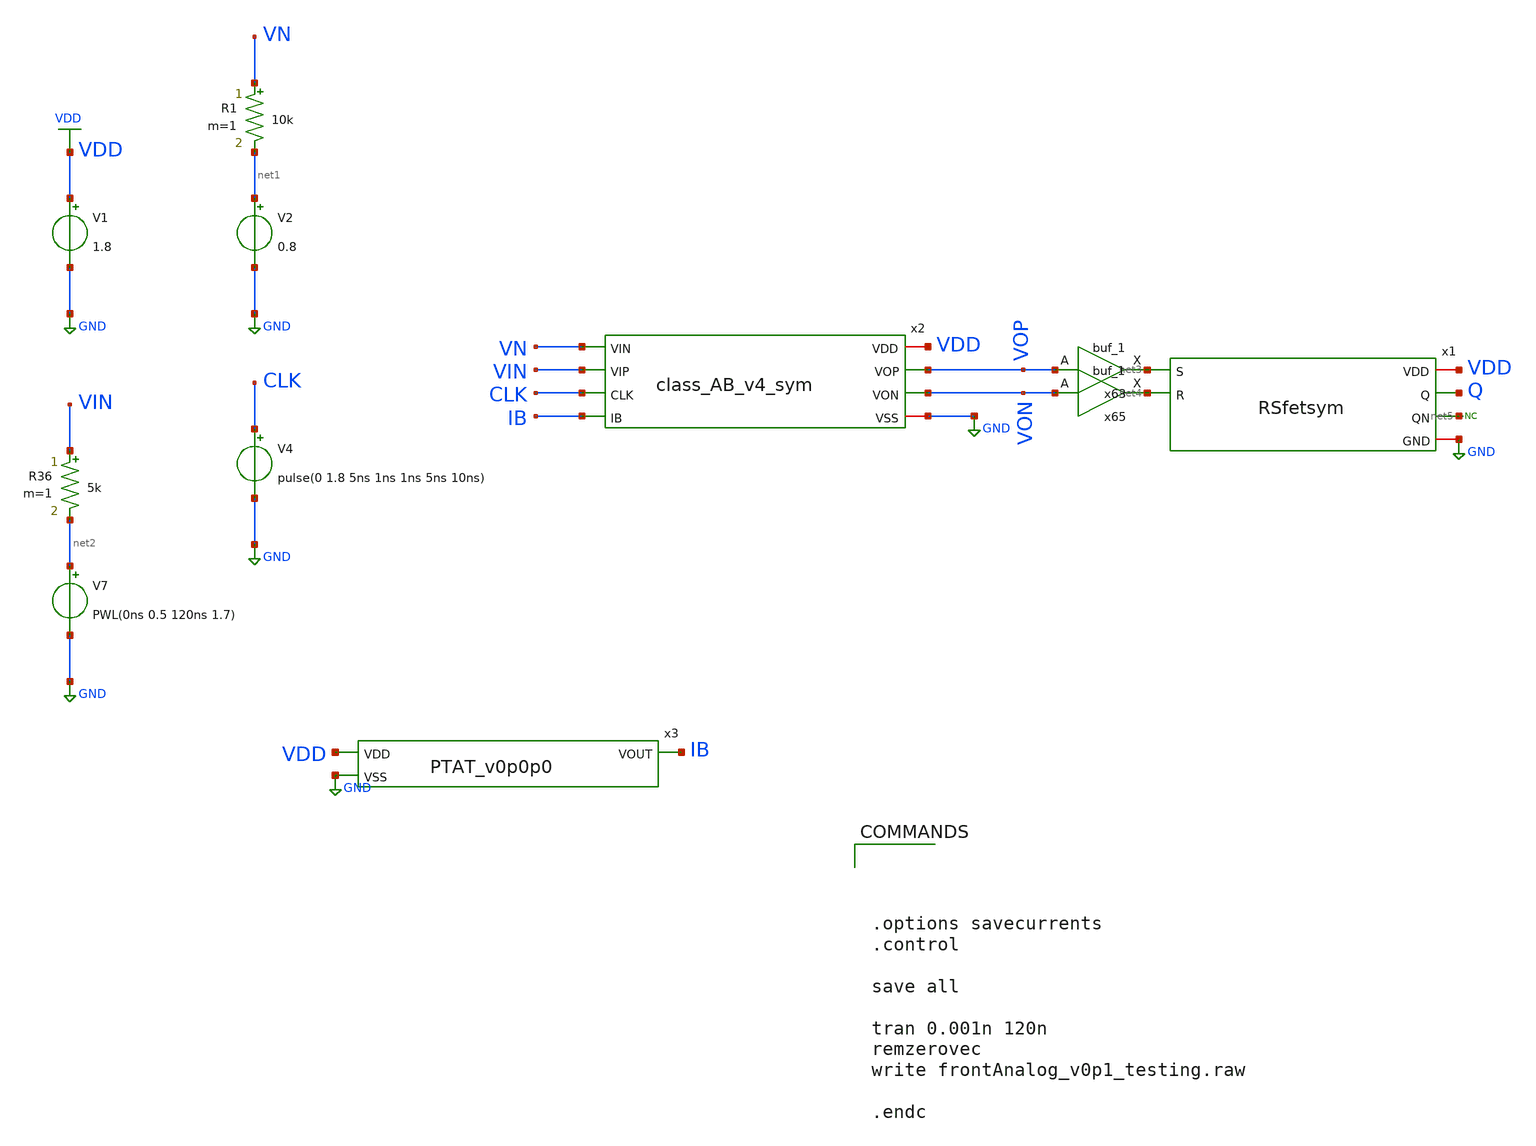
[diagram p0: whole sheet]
** sch_path: flashADC/xschem/frontAnalog_v0p0p1_testing.sch
.lib $::SKYWATER_MODELS/sky130.lib.spice tt
.include $::SKYWATER_STDCELLS/sky130_fd_sc_hd.spice

**.subckt frontAnalog_v0p0p1_testing
x63 VOP GND GND VDD VDD net3 sky130_fd_sc_hd__buf_1
x65 VON GND GND VDD VDD net4 sky130_fd_sc_hd__buf_1
* noconn #net5
x1 VDD net3 net4 Q net5 GND RSfetsym
x2 VDD VON VOP VN VIN CLK IB GND class_AB_v4_sym
V1 VDD GND 1.8
V2 net1 GND 0.8
V4 CLK GND pulse(0 1.8 5ns 1ns 1ns 5ns 10ns)
R1 VN net1 10k m=1
V7 net2 GND PWL(0ns 0.5 120ns 1.7)
R36 VIN net2 5k m=1
x3 VDD IB GND PTAT_v0p0p0
**** begin user architecture code




.options savecurrents
.control

save all

tran 0.001n 120n
remzerovec
write frontAnalog_v0p1_testing.raw

.endc


**** end user architecture code
**.ends
.GLOBAL GND
.GLOBAL VDD
.end
